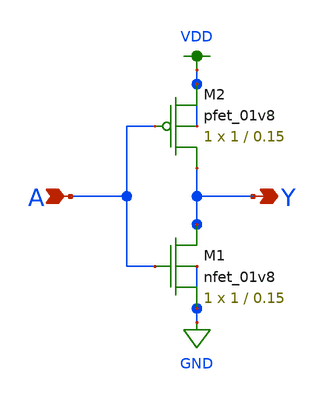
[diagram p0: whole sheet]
** sch_path: simulation/shift_register/andrew_mp2_files/sreg_inverter/sreg_inverter.sch
**.subckt sreg_inverter A Y
*.ipin A
*.opin Y
XM1 Y A GND GND sky130_fd_pr__nfet_01v8 L=0.15 W=1 nf=1 ad='int((nf+1)/2) * W/nf * 0.29' as='int((nf+2)/2) * W/nf * 0.29'
+ pd='2*int((nf+1)/2) * (W/nf + 0.29)' ps='2*int((nf+2)/2) * (W/nf + 0.29)' nrd='0.29 / W' nrs='0.29 / W'
+ sa=0 sb=0 sd=0 mult=1 m=1
XM2 Y A VDD VDD sky130_fd_pr__pfet_01v8 L=0.15 W=1 nf=1 ad='int((nf+1)/2) * W/nf * 0.29' as='int((nf+2)/2) * W/nf * 0.29'
+ pd='2*int((nf+1)/2) * (W/nf + 0.29)' ps='2*int((nf+2)/2) * (W/nf + 0.29)' nrd='0.29 / W' nrs='0.29 / W'
+ sa=0 sb=0 sd=0 mult=1 m=1
**.ends
.GLOBAL VDD
.GLOBAL GND
.end
